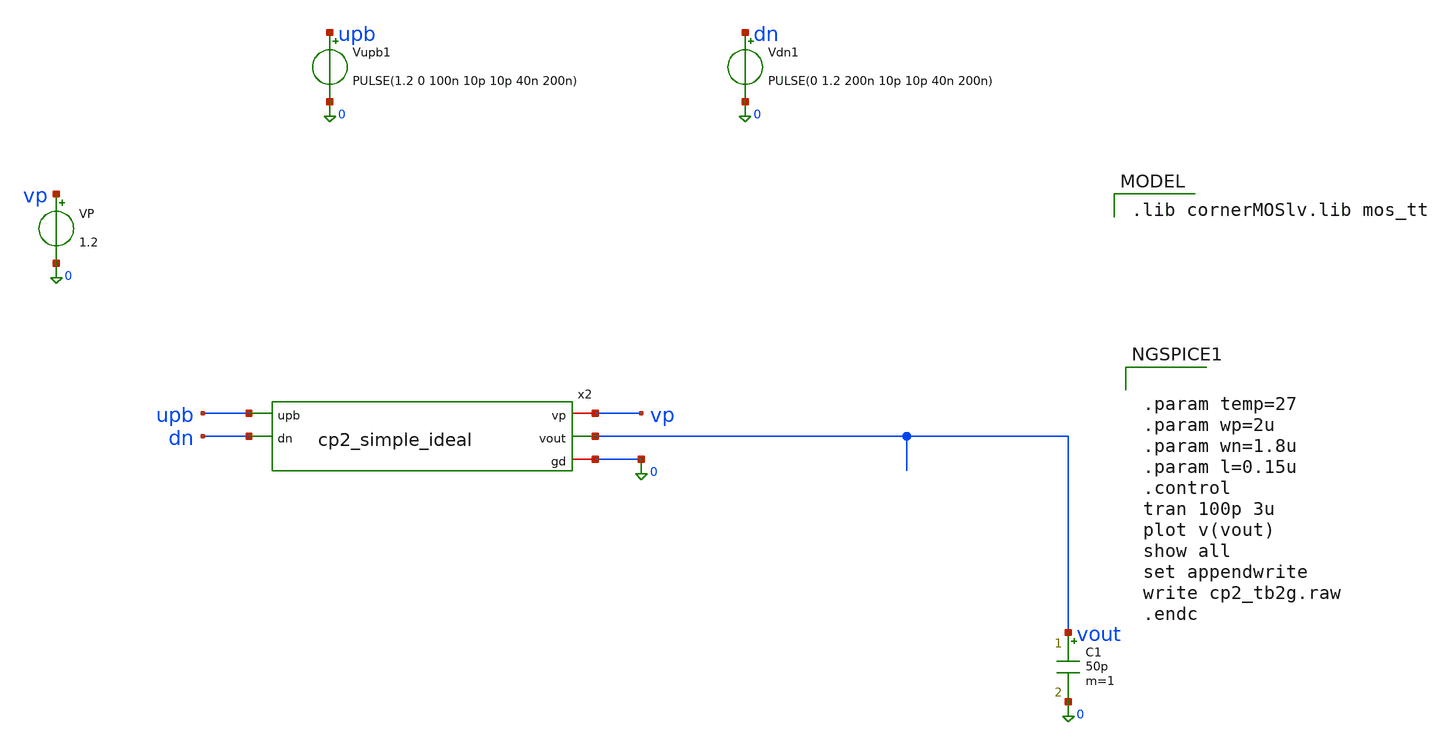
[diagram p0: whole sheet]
** sch_path: charge_pump/cp_v2_tb_missmatch.sch
**.subckt cp_v2_tb_missmatch
C1 vout 0 50p m=1
VP vp 0 1.2
Vupb1 upb 0 PULSE(1.2 0 100n 10p 10p 40n 200n)
Vdn1 dn 0 PULSE(0 1.2 200n 10p 10p 40n 200n)
x2 vp upb vout dn 0 cp2_simple_ideal
**** begin user architecture code
 .lib cornerMOSlv.lib mos_tt



.param temp=27
.param wp=2u
.param wn=1.8u
.param l=0.15u
.control
tran 100p 3u
plot v(vout)
show all
set appendwrite
write cp2_tb2g.raw
.endc


**** end user architecture code
**.ends

* expanding   symbol:  /foss/designs/CHIP-PLL/charge_pump/cp2_simple_ideal.sym # of pins=5
** sym_path: charge_pump/cp2_simple_ideal.sym
** sch_path: charge_pump/cp2_simple_ideal.sch
.subckt cp2_simple_ideal vp upb vout dn gd
*.iopin vp
*.ipin upb
*.opin vout
*.ipin dn
*.iopin gd
XM3 iref_p2 iref_p2 vp vp sg13_lv_pmos w={wp} l={l} ng=1 m=1 mm_ok=1
XM1 net2 iref_p2 vp vp sg13_lv_pmos w={wp} l={l} ng=1 m=1 mm_ok=1
XM6 net3 upb net2 vp sg13_lv_pmos w={wp} l={l} ng=1 m=1 mm_ok=1
XM9 net4 dn net1 gd sg13_lv_nmos w={wn} l={l} ng=1 m=1 mm_ok=1
XM10 net1 iref2 gd gd sg13_lv_nmos w={wn} l={l} ng=1 m=1 mm_ok=1
XM14 iref2 iref2 gd gd sg13_lv_nmos w={wn} l={l} ng=1 m=1 mm_ok=1
Itest1 iref_p2 gd 25u
Itest2 vp iref2 26.9u
Vidn vout net4 0
Viup net3 vout 0
.ends

.end
